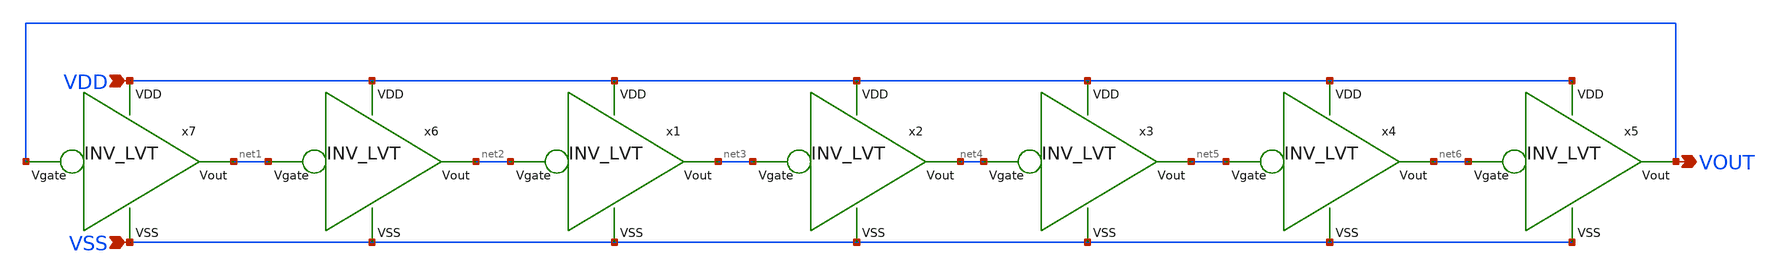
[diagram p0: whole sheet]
** sch_path: design/THESIS_EXP_RO_INVERTER_SKY130A/RO_LVT.sch
**.subckt RO_LVT VDD VSS VOUT
*.ipin VDD
*.ipin VSS
*.opin VOUT
x1 VDD net2 net3 VSS INV_LVT
x2 VDD net3 net4 VSS INV_LVT
x3 VDD net4 net5 VSS INV_LVT
x4 VDD net5 net6 VSS INV_LVT
x5 VDD net6 VOUT VSS INV_LVT
x6 VDD net1 net2 VSS INV_LVT
x7 VDD VOUT net1 VSS INV_LVT
**.ends
.end
